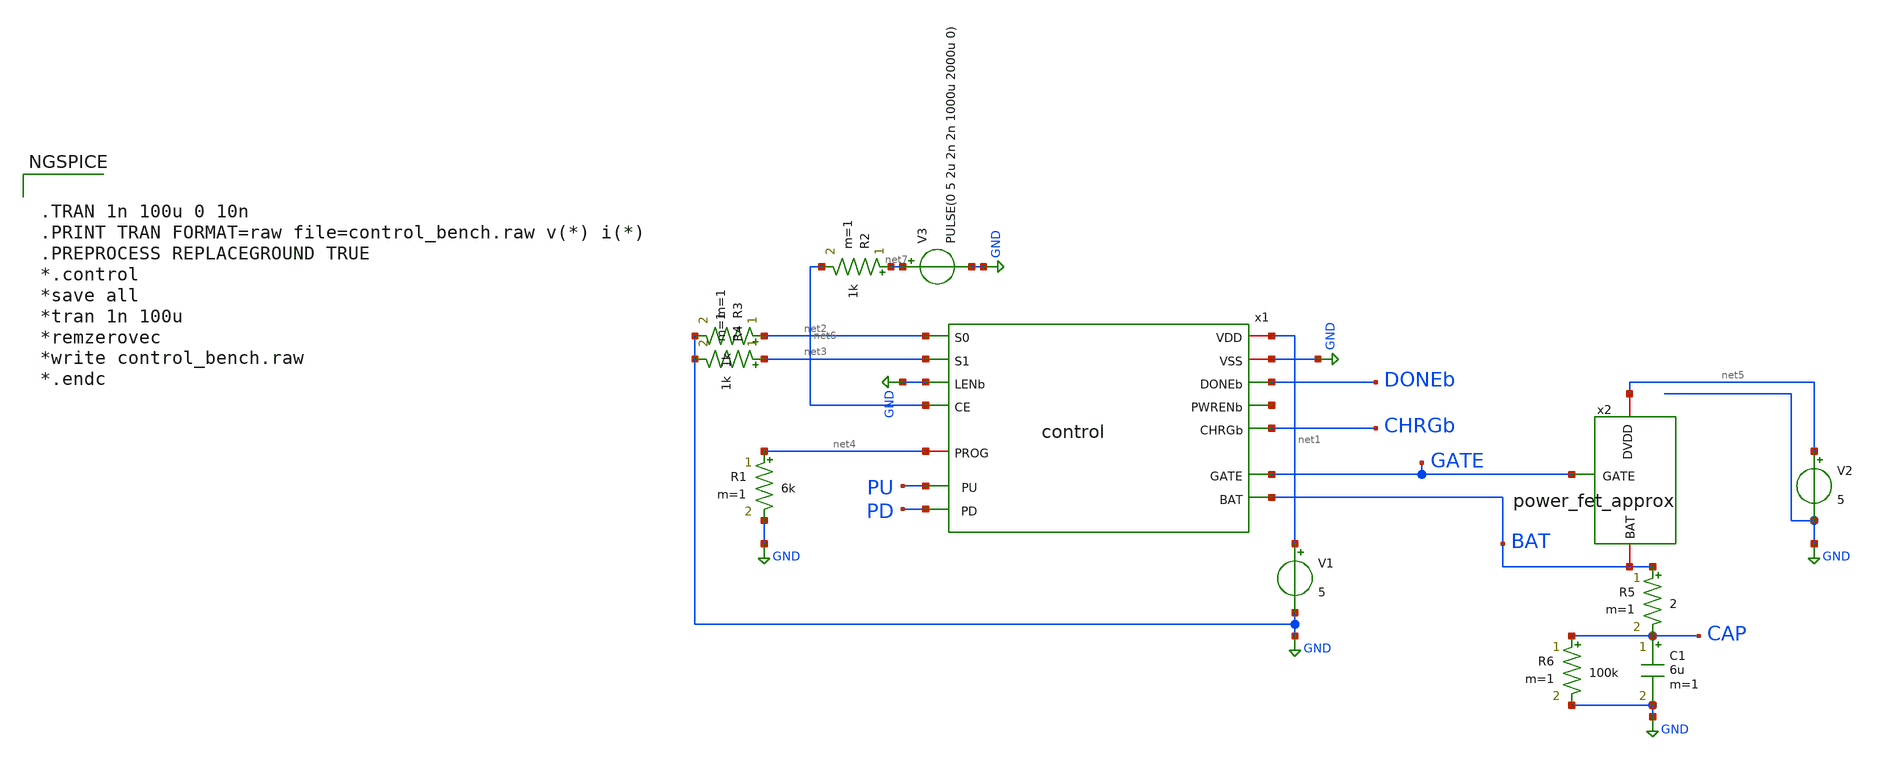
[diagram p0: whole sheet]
** sch_path: analog/xschem/control_bench.sch
**.subckt control_bench
x1 net1 GND net2 DONEb net3 GND net8 net6 BAT CHRGb net4 GATE PU PD control
V1 net1 GND 5
R1 net4 GND 6k m=1
R2 net7 net6 1k m=1
V2 net5 GND 5
R3 net2 GND 1k m=1
R4 net3 GND 1k m=1
V3 net7 GND PULSE(0 5 2u 2n 2n 1000u 2000u 0)
C1 CAP GND 6u m=1
R5 BAT CAP 2 m=1
R6 CAP GND 100k m=1
x2 net5 GATE BAT power_fet_approx
**** begin user architecture code


.TRAN 1n 100u 0 10n
.PRINT TRAN FORMAT=raw file=control_bench.raw v(*) i(*)
.PREPROCESS REPLACEGROUND TRUE
*.control
*save all
*tran 1n 100u
*remzerovec
*write control_bench.raw
*.endc



.include $::PDK_ROOT/gf180mcuD/libs.tech/xyce/design.xyce
.lib $::PDK_ROOT/gf180mcuD/libs.tech/xyce/sm141064.xyce typical
.lib $::PDK_ROOT/gf180mcuD/libs.tech/xyce/sm141064.xyce res_typical
.lib $::PDK_ROOT/gf180mcuD/libs.tech/xyce/sm141064.xyce diode_typical
.lib $::PDK_ROOT/gf180mcuD/libs.tech/xyce/sm141064.xyce mimcap_typical
.lib $::PDK_ROOT/gf180mcuD/libs.tech/xyce/sm141064.xyce cap_mim
.include /run/media/veracrypt1/ws-charge-controller/analog/xschem/extracted/power_fet_f.spice

**** end user architecture code
**.ends
.GLOBAL GND
.end
